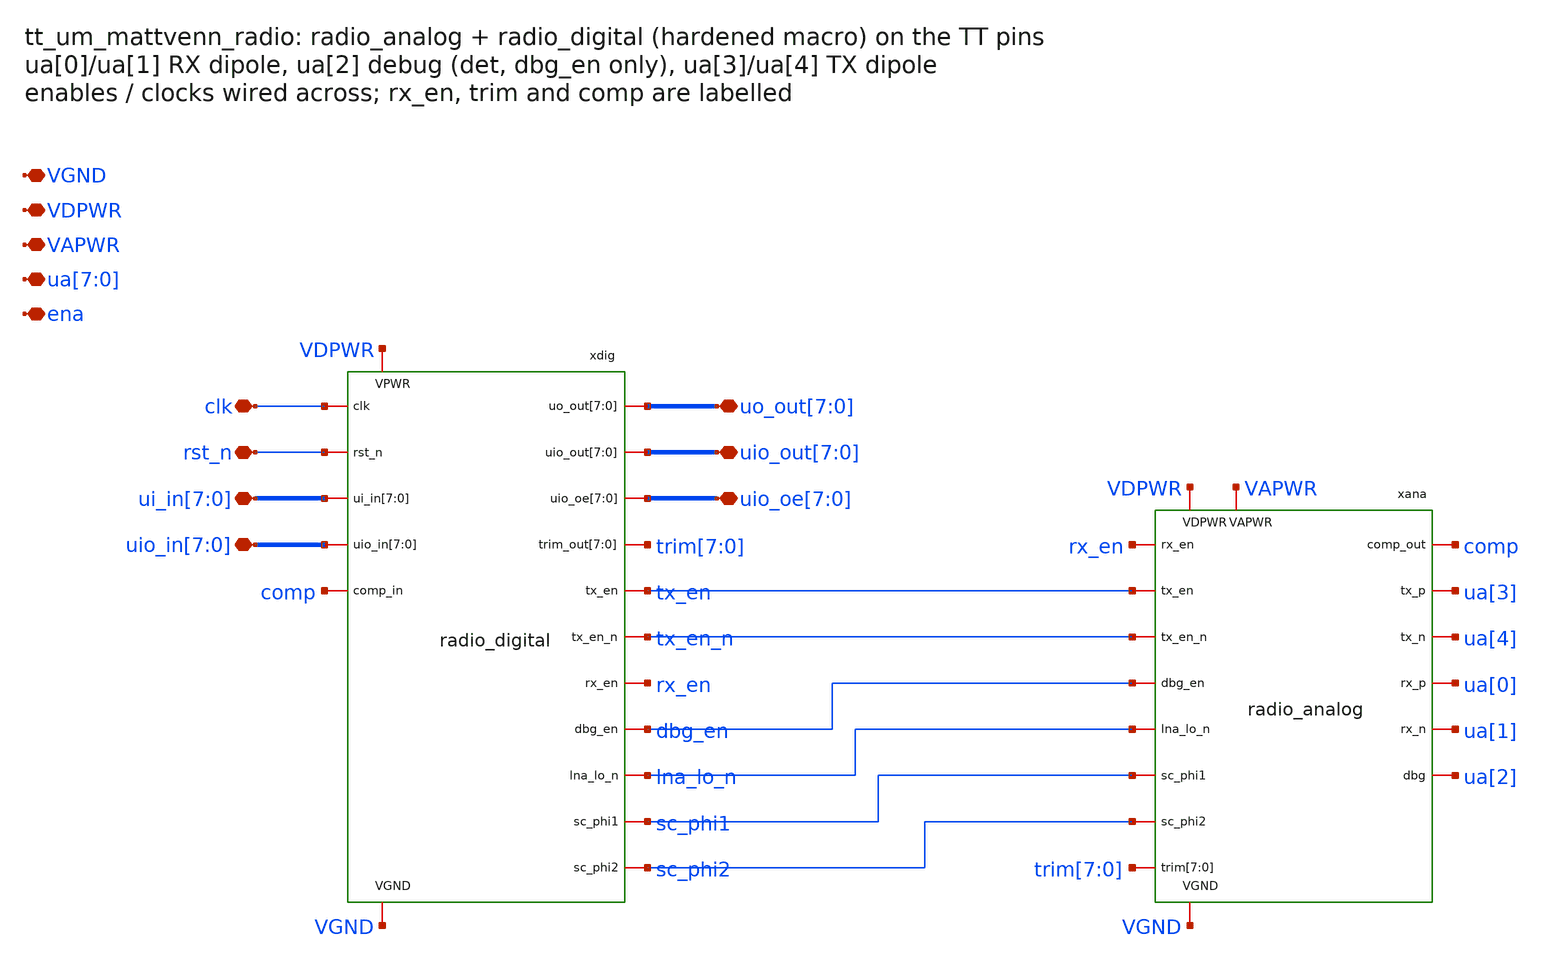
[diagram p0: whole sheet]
** sch_path: xschem/tt_um_mattvenn_radio.sch
**.subckt tt_um_mattvenn_radio VGND VDPWR VAPWR
*+ ui_in[7],ui_in[6],ui_in[5],ui_in[4],ui_in[3],ui_in[2],ui_in[1],ui_in[0] uo_out[7],uo_out[6],uo_out[5],uo_out[4],uo_out[3],uo_out[2],uo_out[1],uo_out[0]
*+ uio_in[7],uio_in[6],uio_in[5],uio_in[4],uio_in[3],uio_in[2],uio_in[1],uio_in[0] uio_out[7],uio_out[6],uio_out[5],uio_out[4],uio_out[3],uio_out[2],uio_out[1],uio_out[0]
*+ uio_oe[7],uio_oe[6],uio_oe[5],uio_oe[4],uio_oe[3],uio_oe[2],uio_oe[1],uio_oe[0] ua[7],ua[6],ua[5],ua[4],ua[3],ua[2],ua[1],ua[0] ena clk rst_n
*.iopin VGND
*.iopin VDPWR
*.iopin VAPWR
*.iopin ui_in[7],ui_in[6],ui_in[5],ui_in[4],ui_in[3],ui_in[2],ui_in[1],ui_in[0]
*.iopin uo_out[7],uo_out[6],uo_out[5],uo_out[4],uo_out[3],uo_out[2],uo_out[1],uo_out[0]
*.iopin uio_in[7],uio_in[6],uio_in[5],uio_in[4],uio_in[3],uio_in[2],uio_in[1],uio_in[0]
*.iopin uio_out[7],uio_out[6],uio_out[5],uio_out[4],uio_out[3],uio_out[2],uio_out[1],uio_out[0]
*.iopin uio_oe[7],uio_oe[6],uio_oe[5],uio_oe[4],uio_oe[3],uio_oe[2],uio_oe[1],uio_oe[0]
*.iopin ua[7],ua[6],ua[5],ua[4],ua[3],ua[2],ua[1],ua[0]
*.iopin ena
*.iopin clk
*.iopin rst_n
xdig clk rst_n ui_in[7] ui_in[6] ui_in[5] ui_in[4] ui_in[3] ui_in[2] ui_in[1] ui_in[0] uio_in[7]
+ uio_in[6] uio_in[5] uio_in[4] uio_in[3] uio_in[2] uio_in[1] uio_in[0] comp uo_out[7] uo_out[6] uo_out[5]
+ uo_out[4] uo_out[3] uo_out[2] uo_out[1] uo_out[0] uio_out[7] uio_out[6] uio_out[5] uio_out[4] uio_out[3]
+ uio_out[2] uio_out[1] uio_out[0] uio_oe[7] uio_oe[6] uio_oe[5] uio_oe[4] uio_oe[3] uio_oe[2] uio_oe[1]
+ uio_oe[0] trim[7] trim[6] trim[5] trim[4] trim[3] trim[2] trim[1] trim[0] tx_en tx_en_n rx_en dbg_en lna_lo_n
+ sc_phi1 sc_phi2 VDPWR VGND radio_digital
xana rx_en tx_en tx_en_n dbg_en lna_lo_n sc_phi1 sc_phi2 trim[7] trim[6] trim[5] trim[4] trim[3]
+ trim[2] trim[1] trim[0] comp ua[3] ua[4] ua[0] ua[1] ua[2] VDPWR VAPWR VGND radio_analog
**.ends

* expanding   symbol:  radio_digital.sym # of pins=18
** sym_path: xschem/radio_digital.sym
** radio_digital: hardened macro (openlane/radio_digital); gate-level netlist from the OpenLane run

* expanding   symbol:  radio_analog.sym # of pins=17
** sym_path: xschem/radio_analog.sym
** sch_path: xschem/radio_analog.sch
.subckt radio_analog rx_en tx_en tx_en_n dbg_en lna_lo_n sc_phi1 sc_phi2 trim[7] trim[6] trim[5]
+ trim[4] trim[3] trim[2] trim[1] trim[0] comp_out tx_p tx_n rx_p rx_n dbg VDPWR VAPWR VGND
*.iopin VDPWR
*.iopin VAPWR
*.iopin VGND
*.iopin rx_en
*.iopin tx_en
*.iopin tx_en_n
*.iopin dbg_en
*.iopin lna_lo_n
*.iopin sc_phi1
*.iopin sc_phi2
*.iopin trim[7],trim[6],trim[5],trim[4],trim[3],trim[2],trim[1],trim[0]
*.iopin comp_out
*.iopin tx_p
*.iopin tx_n
*.iopin rx_p
*.iopin rx_n
*.iopin dbg
xbias rx_en vcm ib_chain ib_det ib_comp VDPWR VGND bias_gen rref=10k rdiv=200k rtail=250k wpu=2
+ cc=1p
xchain rx_p rx_n ib_chain vcm lna_lo_n out_p out_n o1p o1n o2p o2n o3p o3n o4p o4n o5p o5n VDPWR
+ VGND lna_chain w1=80 rl1=1k mt1=20 w2=20 rl2=4k mt2=6 cs=0.6p cin=2p rb=20k mm=0
xdet o1p o1n o2p o2n o3p o3n o4p o4n o5p o5n out_p out_n ib_det det VDPWR VGND log_det wd=1 rs=10k
+ cc=100f rb=200k rdet=8k cdet=5p
xlpf det lpf VGND lpf_rc lr=136 nc=6
xavg lpf sc_phi1 sc_phi2 avg VDPWR VGND avg_sc ncs=1 nca=5
xdac trim[0] trim[1] trim[2] trim[3] trim[4] trim[5] trim[6] trim[7] trim VGND r2r
XCtrim trim VGND sky130_fd_pr__cap_mim_m3_1 W='sqrt((1e-12)/1/2.06e-15)' L='sqrt((1e-12)/1/2.06e-15)'
+ MF=1 m=1
xcomp avg lpf trim ib_comp comp_out VDPWR VGND comp_ct w1=20 l1=1 mt1=10 rdeg=0.85Meg mta=2 lref1=68
+ lref2=204 wcl=22
xdbg det dbg_en dbg VDPWR VGND dbg_tg wn=2 wp=4
xtx tx_en tx_en tx_en_n tx_p tx_n VDPWR VAPWR VGND tx_top
xdeca VAPWR VGND decap_vapwr
xdecd VDPWR VGND decap_vdpwr
.ends


* expanding   symbol:  bias_gen.sym # of pins=7
** sym_path: xschem/bias_gen.sym
** sch_path: xschem/bias_gen.sch
.subckt bias_gen en vcm ib_chain ib_det ib_comp VDD VSS  rref=10k rdiv=200k rtail=250k wpu=2 cc=1p
*.iopin VDD
*.iopin VSS
*.iopin en
*.iopin vcm
*.iopin ib_chain
*.iopin ib_det
*.iopin ib_comp
XMeip enb en VDD VDD sky130_fd_pr__pfet_01v8 L=0.15 W=1 nf=1 ad='int((nf+1)/2) * W/nf * 0.29' as='int((nf+2)/2) * W/nf * 0.29'
+ pd='2*int((nf+1)/2) * (W/nf + 0.29)' ps='2*int((nf+2)/2) * (W/nf + 0.29)' nrd='0.29 / W' nrs='0.29 / W'
+ sa=0 sb=0 sd=0 mult=1 m=1
XMein enb en VSS VSS sky130_fd_pr__nfet_01v8 L=0.15 W=0.5 nf=1 ad='int((nf+1)/2) * W/nf * 0.29' as='int((nf+2)/2) * W/nf * 0.29'
+ pd='2*int((nf+1)/2) * (W/nf + 0.29)' ps='2*int((nf+2)/2) * (W/nf + 0.29)' nrd='0.29 / W' nrs='0.29 / W'
+ sa=0 sb=0 sd=0 mult=1 m=1
XRd1 vcm VDD VSS sky130_fd_pr__res_xhigh_po_0p35 L='max((rdiv-0)/7379,0.5)' mult=1 m=1
XRd2 vref vcm VSS sky130_fd_pr__res_xhigh_po_0p35 L='max((rdiv-0)/7379,0.5)' mult=1 m=1
XRd3 dsw vref VSS sky130_fd_pr__res_xhigh_po_0p35 L='max((rdiv-0)/7379,0.5)' mult=1 m=1
XMdsw dsw en VSS VSS sky130_fd_pr__nfet_01v8 L=0.15 W=1 nf=1 ad='int((nf+1)/2) * W/nf * 0.29' as='int((nf+2)/2) * W/nf * 0.29'
+ pd='2*int((nf+1)/2) * (W/nf + 0.29)' ps='2*int((nf+2)/2) * (W/nf + 0.29)' nrd='0.29 / W' nrs='0.29 / W'
+ sa=0 sb=0 sd=0 mult=1 m=1
XCvcm vcm VSS sky130_fd_pr__cap_mim_m3_1 W='sqrt((2e-12)/2/2.06e-15)' L='sqrt((2e-12)/2/2.06e-15)' MF=2
+ m=2
XCvref vref VSS sky130_fd_pr__cap_mim_m3_1 W='sqrt((2e-12)/2/2.06e-15)' L='sqrt((2e-12)/2/2.06e-15)'
+ MF=2 m=2
XMpb pb pb VDD VDD sky130_fd_pr__pfet_01v8 L=1 W=4 nf=1 ad='int((nf+1)/2) * W/nf * 0.29' as='int((nf+2)/2) * W/nf * 0.29'
+ pd='2*int((nf+1)/2) * (W/nf + 0.29)' ps='2*int((nf+2)/2) * (W/nf + 0.29)' nrd='0.29 / W' nrs='0.29 / W'
+ sa=0 sb=0 sd=0 mult=1 m=1
XRtail tsw pb VSS sky130_fd_pr__res_xhigh_po_0p35 L='max((rtail-0)/7379,0.5)' mult=1 m=1
XMtsw tsw en VSS VSS sky130_fd_pr__nfet_01v8 L=0.15 W=1 nf=1 ad='int((nf+1)/2) * W/nf * 0.29' as='int((nf+2)/2) * W/nf * 0.29'
+ pd='2*int((nf+1)/2) * (W/nf + 0.29)' ps='2*int((nf+2)/2) * (W/nf + 0.29)' nrd='0.29 / W' nrs='0.29 / W'
+ sa=0 sb=0 sd=0 mult=1 m=1
XMpt tail pb VDD VDD sky130_fd_pr__pfet_01v8 L=1 W=4 nf=1 ad='int((nf+1)/2) * W/nf * 0.29' as='int((nf+2)/2) * W/nf * 0.29'
+ pd='2*int((nf+1)/2) * (W/nf + 0.29)' ps='2*int((nf+2)/2) * (W/nf + 0.29)' nrd='0.29 / W' nrs='0.29 / W'
+ sa=0 sb=0 sd=0 mult=1 m=1
XM1 d1 vref tail VDD sky130_fd_pr__pfet_01v8 L=1 W=4 nf=1 ad='int((nf+1)/2) * W/nf * 0.29' as='int((nf+2)/2) * W/nf * 0.29'
+ pd='2*int((nf+1)/2) * (W/nf + 0.29)' ps='2*int((nf+2)/2) * (W/nf + 0.29)' nrd='0.29 / W' nrs='0.29 / W'
+ sa=0 sb=0 sd=0 mult=1 m=1
XM2 ota x tail VDD sky130_fd_pr__pfet_01v8 L=1 W=4 nf=1 ad='int((nf+1)/2) * W/nf * 0.29' as='int((nf+2)/2) * W/nf * 0.29'
+ pd='2*int((nf+1)/2) * (W/nf + 0.29)' ps='2*int((nf+2)/2) * (W/nf + 0.29)' nrd='0.29 / W' nrs='0.29 / W'
+ sa=0 sb=0 sd=0 mult=1 m=1
XM3 d1 d1 VSS VSS sky130_fd_pr__nfet_01v8 L=2 W=2 nf=1 ad='int((nf+1)/2) * W/nf * 0.29' as='int((nf+2)/2) * W/nf * 0.29'
+ pd='2*int((nf+1)/2) * (W/nf + 0.29)' ps='2*int((nf+2)/2) * (W/nf + 0.29)' nrd='0.29 / W' nrs='0.29 / W'
+ sa=0 sb=0 sd=0 mult=1 m=1
XM4 ota d1 VSS VSS sky130_fd_pr__nfet_01v8 L=2 W=2 nf=1 ad='int((nf+1)/2) * W/nf * 0.29' as='int((nf+2)/2) * W/nf * 0.29'
+ pd='2*int((nf+1)/2) * (W/nf + 0.29)' ps='2*int((nf+2)/2) * (W/nf + 0.29)' nrd='0.29 / W' nrs='0.29 / W'
+ sa=0 sb=0 sd=0 mult=1 m=1
XCc ota VSS sky130_fd_pr__cap_mim_m3_1 W='sqrt((cc)/1/2.06e-15)' L='sqrt((cc)/1/2.06e-15)' MF=1 m=1
XMpd ota enb VSS VSS sky130_fd_pr__nfet_01v8 L=0.15 W=1 nf=1 ad='int((nf+1)/2) * W/nf * 0.29' as='int((nf+2)/2) * W/nf * 0.29'
+ pd='2*int((nf+1)/2) * (W/nf + 0.29)' ps='2*int((nf+2)/2) * (W/nf + 0.29)' nrd='0.29 / W' nrs='0.29 / W'
+ sa=0 sb=0 sd=0 mult=1 m=1
XMn pr ota x VSS sky130_fd_pr__nfet_01v8 L=0.5 W=20 nf=2 ad='int((nf+1)/2) * W/nf * 0.29' as='int((nf+2)/2) * W/nf * 0.29'
+ pd='2*int((nf+1)/2) * (W/nf + 0.29)' ps='2*int((nf+2)/2) * (W/nf + 0.29)' nrd='0.29 / W' nrs='0.29 / W'
+ sa=0 sb=0 sd=0 mult=1 m=1
XRref1 xr x VSS sky130_fd_pr__res_high_po_0p69 L='max((rref/2-526)/470.9,0.5)' mult=1 m=1
XRref2 VSS xr VSS sky130_fd_pr__res_high_po_0p69 L='max((rref/2-526)/470.9,0.5)' mult=1 m=1
XMpr pr pr VDD VDD sky130_fd_pr__pfet_01v8 L=1 W='wpu' nf=1 ad='int((nf+1)/2) * W/nf * 0.29' as='int((nf+2)/2) * W/nf * 0.29'
+ pd='2*int((nf+1)/2) * (W/nf + 0.29)' ps='2*int((nf+2)/2) * (W/nf + 0.29)' nrd='0.29 / W' nrs='0.29 / W'
+ sa=0 sb=0 sd=0 mult=60 m=60
XMpu pr en VDD VDD sky130_fd_pr__pfet_01v8 L=0.15 W=1 nf=1 ad='int((nf+1)/2) * W/nf * 0.29' as='int((nf+2)/2) * W/nf * 0.29'
+ pd='2*int((nf+1)/2) * (W/nf + 0.29)' ps='2*int((nf+2)/2) * (W/nf + 0.29)' nrd='0.29 / W' nrs='0.29 / W'
+ sa=0 sb=0 sd=0 mult=1 m=1
XMo_ib_chain ib_chain pr VDD VDD sky130_fd_pr__pfet_01v8 L=1 W='wpu' nf=1 ad='int((nf+1)/2) * W/nf * 0.29'
+ as='int((nf+2)/2) * W/nf * 0.29' pd='2*int((nf+1)/2) * (W/nf + 0.29)' ps='2*int((nf+2)/2) * (W/nf + 0.29)'
+ nrd='0.29 / W' nrs='0.29 / W' sa=0 sb=0 sd=0 mult=60 m=60
XMo_ib_det ib_det pr VDD VDD sky130_fd_pr__pfet_01v8 L=1 W='wpu' nf=1 ad='int((nf+1)/2) * W/nf * 0.29'
+ as='int((nf+2)/2) * W/nf * 0.29' pd='2*int((nf+1)/2) * (W/nf + 0.29)' ps='2*int((nf+2)/2) * (W/nf + 0.29)'
+ nrd='0.29 / W' nrs='0.29 / W' sa=0 sb=0 sd=0 mult=2 m=2
XMo_ib_comp ib_comp pr VDD VDD sky130_fd_pr__pfet_01v8 L=1 W='wpu' nf=1 ad='int((nf+1)/2) * W/nf * 0.29'
+ as='int((nf+2)/2) * W/nf * 0.29' pd='2*int((nf+1)/2) * (W/nf + 0.29)' ps='2*int((nf+2)/2) * (W/nf + 0.29)'
+ nrd='0.29 / W' nrs='0.29 / W' sa=0 sb=0 sd=0 mult=1 m=1
XMdum VDD VDD VDD VDD sky130_fd_pr__pfet_01v8 L=1 W='wpu' nf=1 ad='int((nf+1)/2) * W/nf * 0.29' as='int((nf+2)/2) * W/nf * 0.29'
+ pd='2*int((nf+1)/2) * (W/nf + 0.29)' ps='2*int((nf+2)/2) * (W/nf + 0.29)' nrd='0.29 / W' nrs='0.29 / W'
+ sa=0 sb=0 sd=0 mult=5 m=5
.ends


* expanding   symbol:  lna_chain.sym # of pins=19
** sym_path: xschem/lna_chain.sym
** sch_path: xschem/lna_chain.sch
.subckt lna_chain inp inn ibias vcm lna_lo_n outp outn o1p o1n o2p o2n o3p o3n o4p o4n o5p o5n VDD
+ VSS  w1=80 rl1=1k mt1=20 w2=20 rl2=4k mt2=6 cs=0.6p cin=2p rb=20k mm=0
*.iopin VDD
*.iopin VSS
*.iopin ibias
*.iopin vcm
*.iopin lna_lo_n
*.iopin inp
*.iopin inn
*.iopin outp
*.iopin outn
*.iopin o1p
*.iopin o1n
*.iopin o2p
*.iopin o2n
*.iopin o3p
*.iopin o3n
*.iopin o4p
*.iopin o4n
*.iopin o5p
*.iopin o5n
XMref ibias ibias VSS VSS sky130_fd_pr__nfet_01v8 L=0.5 W=6 nf=2 ad='int((nf+1)/2) * W/nf * 0.29' as='int((nf+2)/2) * W/nf * 0.29'
+ pd='2*int((nf+1)/2) * (W/nf + 0.29)' ps='2*int((nf+2)/2) * (W/nf + 0.29)' nrd='0.29 / W' nrs='0.29 / W'
+ sa=0 sb=0 sd=0 mult=1 m=1
XCin_p g1p inp sky130_fd_pr__cap_mim_m3_1 W='sqrt((cin)/2.06e-15/3.84131)' L='3.84131*sqrt((cin)/2.06e-15/3.84131)'
+ MF=1 m=1
XRb_p g1p vcm VSS sky130_fd_pr__res_high_po_0p35 L='max((rb-963)/995,0.5)' mult=1 m=1
XCin_n g1n inn sky130_fd_pr__cap_mim_m3_1 W='sqrt((cin)/2.06e-15/3.84131)' L='3.84131*sqrt((cin)/2.06e-15/3.84131)'
+ MF=1 m=1
XRb_n g1n vcm VSS sky130_fd_pr__res_high_po_0p35 L='max((rb-963)/995,0.5)' mult=1 m=1
xa1 g1p g1n ibias o1p o1n VDD VSS amp_dp w='w1' l=0.15 rl='rl1' wt=6 mt='mt1' mm='mm'
xa2 o1p o1n ibias o2p o2n VDD VSS amp_dpc w='w2' l=0.15 rl='rl2' wt=6 mt='mt2' cs='cs'
xa3 o2p o2n ibias o3p o3n VDD VSS amp_dpc w='w2' l=0.15 rl='rl2' wt=6 mt='mt2' cs='cs'
xa4 o3p o3n ibias o4p o4n VDD VSS amp_dpc w='w2' l=0.15 rl='rl2' wt=6 mt='mt2' cs='cs'
xa5 o4p o4n ibias o5p o5n VDD VSS amp_dpc w='w2' l=0.15 rl='rl2' wt=6 mt='mt2' cs='cs'
xa6 o5p o5n ibias outp outn VDD VSS amp_dpc w='w2' l=0.15 rl='rl2' wt=6 mt='mt2' cs='cs'
xsh o2p o2n lna_lo_n VDD VSS lna_shunt rh=421 wsw=18 rg=20k
.ends


* expanding   symbol:  log_det.sym # of pins=16
** sym_path: xschem/log_det.sym
** sch_path: xschem/log_det.sch
.subckt log_det t1p t1n t2p t2n t3p t3n t4p t4n t5p t5n t6p t6n ibias_det det VDD VSS  wd=1 rs=10k
+ cc=100f rb=200k rdet=8k cdet=5p
*.iopin VDD
*.iopin VSS
*.iopin ibias_det
*.iopin det
*.iopin t1p
*.iopin t1n
*.iopin t2p
*.iopin t2n
*.iopin t3p
*.iopin t3n
*.iopin t4p
*.iopin t4n
*.iopin t5p
*.iopin t5n
*.iopin t6p
*.iopin t6n
XMbias ibias_det ibias_det sb VSS sky130_fd_pr__nfet_01v8 L=0.15 W='wd' nf=1 ad='int((nf+1)/2) * W/nf * 0.29'
+ as='int((nf+2)/2) * W/nf * 0.29' pd='2*int((nf+1)/2) * (W/nf + 0.29)' ps='2*int((nf+2)/2) * (W/nf + 0.29)'
+ nrd='0.29 / W' nrs='0.29 / W' sa=0 sb=0 sd=0 mult=1 m=1
XRs_b VSS sb VSS sky130_fd_pr__res_high_po_0p35 L='max((rs-963)/995,0.5)' mult=1 m=1
XRdet det VDD VSS sky130_fd_pr__res_high_po_0p69 L='max((rdet-526)/470.9,0.5)' mult=1 m=1
XCdet det VDD sky130_fd_pr__cap_mim_m3_1 W='sqrt((cdet)/1/2.06e-15)' L='sqrt((cdet)/1/2.06e-15)' MF=1
+ m=1
xd1 t1p t1n ibias_det det VSS det_cell wd='wd' rs='rs' cc='cc' rb='rb'
xd2 t2p t2n ibias_det det VSS det_cell wd='wd' rs='rs' cc='cc' rb='rb'
xd3 t3p t3n ibias_det det VSS det_cell wd='wd' rs='rs' cc='cc' rb='rb'
xd4 t4p t4n ibias_det det VSS det_cell wd='wd' rs='rs' cc='cc' rb='rb'
xd5 t5p t5n ibias_det det VSS det_cell wd='wd' rs='rs' cc='cc' rb='rb'
xd6 t6p t6n ibias_det det VSS det_cell wd='wd' rs='rs' cc='cc' rb='rb'
.ends


* expanding   symbol:  lpf_rc.sym # of pins=3
** sym_path: xschem/lpf_rc.sym
** sch_path: xschem/lpf_rc.sch
.subckt lpf_rc in out VSS  lr=136 nc=6
*.iopin VSS
*.iopin in
*.iopin out
XR1 in out VSS sky130_fd_pr__res_xhigh_po_0p35 L='lr' mult=1 m=1
XC1 out VSS sky130_fd_pr__cap_mim_m3_1 W=30 L=30 MF='nc' m='nc'
.ends


* expanding   symbol:  avg_sc.sym # of pins=6
** sym_path: xschem/avg_sc.sym
** sch_path: xschem/avg_sc.sch
.subckt avg_sc in phi1 phi2 out VDD VSS  ncs=1 nca=5
*.iopin VDD
*.iopin VSS
*.iopin in
*.iopin out
*.iopin phi1
*.iopin phi2
XMiphi1p phi1b phi1 VDD VDD sky130_fd_pr__pfet_01v8 L=0.15 W=1 nf=1 ad='int((nf+1)/2) * W/nf * 0.29'
+ as='int((nf+2)/2) * W/nf * 0.29' pd='2*int((nf+1)/2) * (W/nf + 0.29)' ps='2*int((nf+2)/2) * (W/nf + 0.29)'
+ nrd='0.29 / W' nrs='0.29 / W' sa=0 sb=0 sd=0 mult=1 m=1
XMiphi1n phi1b phi1 VSS VSS sky130_fd_pr__nfet_01v8 L=0.15 W=0.5 nf=1 ad='int((nf+1)/2) * W/nf * 0.29'
+ as='int((nf+2)/2) * W/nf * 0.29' pd='2*int((nf+1)/2) * (W/nf + 0.29)' ps='2*int((nf+2)/2) * (W/nf + 0.29)'
+ nrd='0.29 / W' nrs='0.29 / W' sa=0 sb=0 sd=0 mult=1 m=1
XMiphi2p phi2b phi2 VDD VDD sky130_fd_pr__pfet_01v8 L=0.15 W=1 nf=1 ad='int((nf+1)/2) * W/nf * 0.29'
+ as='int((nf+2)/2) * W/nf * 0.29' pd='2*int((nf+1)/2) * (W/nf + 0.29)' ps='2*int((nf+2)/2) * (W/nf + 0.29)'
+ nrd='0.29 / W' nrs='0.29 / W' sa=0 sb=0 sd=0 mult=1 m=1
XMiphi2n phi2b phi2 VSS VSS sky130_fd_pr__nfet_01v8 L=0.15 W=0.5 nf=1 ad='int((nf+1)/2) * W/nf * 0.29'
+ as='int((nf+2)/2) * W/nf * 0.29' pd='2*int((nf+1)/2) * (W/nf + 0.29)' ps='2*int((nf+2)/2) * (W/nf + 0.29)'
+ nrd='0.29 / W' nrs='0.29 / W' sa=0 sb=0 sd=0 mult=1 m=1
XS1n in phi1 cs VSS sky130_fd_pr__nfet_01v8 L=0.15 W=0.5 nf=1 ad='int((nf+1)/2) * W/nf * 0.29' as='int((nf+2)/2) * W/nf * 0.29'
+ pd='2*int((nf+1)/2) * (W/nf + 0.29)' ps='2*int((nf+2)/2) * (W/nf + 0.29)' nrd='0.29 / W' nrs='0.29 / W'
+ sa=0 sb=0 sd=0 mult=1 m=1
XS1p in phi1b cs VDD sky130_fd_pr__pfet_01v8 L=0.15 W=1 nf=1 ad='int((nf+1)/2) * W/nf * 0.29' as='int((nf+2)/2) * W/nf * 0.29'
+ pd='2*int((nf+1)/2) * (W/nf + 0.29)' ps='2*int((nf+2)/2) * (W/nf + 0.29)' nrd='0.29 / W' nrs='0.29 / W'
+ sa=0 sb=0 sd=0 mult=1 m=1
XS2n cs phi2 out VSS sky130_fd_pr__nfet_01v8 L=0.15 W=0.5 nf=1 ad='int((nf+1)/2) * W/nf * 0.29' as='int((nf+2)/2) * W/nf * 0.29'
+ pd='2*int((nf+1)/2) * (W/nf + 0.29)' ps='2*int((nf+2)/2) * (W/nf + 0.29)' nrd='0.29 / W' nrs='0.29 / W'
+ sa=0 sb=0 sd=0 mult=1 m=1
XS2p cs phi2b out VDD sky130_fd_pr__pfet_01v8 L=0.15 W=1 nf=1 ad='int((nf+1)/2) * W/nf * 0.29' as='int((nf+2)/2) * W/nf * 0.29'
+ pd='2*int((nf+1)/2) * (W/nf + 0.29)' ps='2*int((nf+2)/2) * (W/nf + 0.29)' nrd='0.29 / W' nrs='0.29 / W'
+ sa=0 sb=0 sd=0 mult=1 m=1
XCs cs VSS sky130_fd_pr__cap_mim_m3_1 W='wcs' L='wcs' MF='ncs' m='ncs'
XCavg out VSS sky130_fd_pr__cap_mim_m3_1 W=30 L=30 MF='nca' m='nca'
.ends


* expanding   symbol:  r2r.sym # of pins=10
** sym_path: xschem/r2r.sym
** sch_path: xschem/r2r.sch
.subckt r2r b0 b1 b2 b3 b4 b5 b6 b7 out VGND
*.iopin b0
*.iopin b1
*.iopin b2
*.iopin b3
*.iopin b4
*.iopin b5
*.iopin b6
*.iopin b7
*.iopin out
*.iopin VGND
XR1 s0 b0 VGND sky130_fd_pr__res_high_po_1p41 L=45 mult=1 m=1
XR2 a0 s0 VGND sky130_fd_pr__res_high_po_1p41 L=45 mult=1 m=1
XR3 s1 a0 VGND sky130_fd_pr__res_high_po_1p41 L=45 mult=1 m=1
XR4 VGND s1 VGND sky130_fd_pr__res_high_po_1p41 L=45 mult=1 m=1
XR5 VGND VGND VGND sky130_fd_pr__res_high_po_1p41 L=45 mult=1 m=1
XR6 a1 a0 VGND sky130_fd_pr__res_high_po_1p41 L=45 mult=1 m=1
XR7 t1 a1 VGND sky130_fd_pr__res_high_po_1p41 L=45 mult=1 m=1
XR8 b1 t1 VGND sky130_fd_pr__res_high_po_1p41 L=45 mult=1 m=1
XR9 a2 a1 VGND sky130_fd_pr__res_high_po_1p41 L=45 mult=1 m=1
XR10 t2 a2 VGND sky130_fd_pr__res_high_po_1p41 L=45 mult=1 m=1
XR11 b2 t2 VGND sky130_fd_pr__res_high_po_1p41 L=45 mult=1 m=1
XR12 a3 a2 VGND sky130_fd_pr__res_high_po_1p41 L=45 mult=1 m=1
XR13 t3 a3 VGND sky130_fd_pr__res_high_po_1p41 L=45 mult=1 m=1
XR14 b3 t3 VGND sky130_fd_pr__res_high_po_1p41 L=45 mult=1 m=1
XR15 a4 a3 VGND sky130_fd_pr__res_high_po_1p41 L=45 mult=1 m=1
XR16 t4 a4 VGND sky130_fd_pr__res_high_po_1p41 L=45 mult=1 m=1
XR17 b4 t4 VGND sky130_fd_pr__res_high_po_1p41 L=45 mult=1 m=1
XR18 a5 a4 VGND sky130_fd_pr__res_high_po_1p41 L=45 mult=1 m=1
XR19 t5 a5 VGND sky130_fd_pr__res_high_po_1p41 L=45 mult=1 m=1
XR20 b5 t5 VGND sky130_fd_pr__res_high_po_1p41 L=45 mult=1 m=1
XR21 a6 a5 VGND sky130_fd_pr__res_high_po_1p41 L=45 mult=1 m=1
XR22 t6 a6 VGND sky130_fd_pr__res_high_po_1p41 L=45 mult=1 m=1
XR23 b6 t6 VGND sky130_fd_pr__res_high_po_1p41 L=45 mult=1 m=1
XR24 out a6 VGND sky130_fd_pr__res_high_po_1p41 L=45 mult=1 m=1
XR25 t7 out VGND sky130_fd_pr__res_high_po_1p41 L=45 mult=1 m=1
XR26 b7 t7 VGND sky130_fd_pr__res_high_po_1p41 L=45 mult=1 m=1
XR27 VGND VGND VGND sky130_fd_pr__res_high_po_1p41 L=45 mult=1 m=1
.ends


* expanding   symbol:  comp_ct.sym # of pins=7
** sym_path: xschem/comp_ct.sym
** sch_path: xschem/comp_ct.sch
.subckt comp_ct inp inn trim ibias out VDD VSS  w1=20 l1=1 mt1=10 rdeg=0.85Meg mta=2 lref1=68
+ lref2=204 wcl=22
*.iopin VDD
*.iopin VSS
*.iopin ibias
*.iopin inp
*.iopin inn
*.iopin trim
*.iopin out
XMb ibias ibias VSS VSS sky130_fd_pr__nfet_01v8 L=2 W=2 nf=1 ad='int((nf+1)/2) * W/nf * 0.29' as='int((nf+2)/2) * W/nf * 0.29'
+ pd='2*int((nf+1)/2) * (W/nf + 0.29)' ps='2*int((nf+2)/2) * (W/nf + 0.29)' nrd='0.29 / W' nrs='0.29 / W'
+ sa=0 sb=0 sd=0 mult=1 m=1
XMt1 tail ibias VSS VSS sky130_fd_pr__nfet_01v8 L=2 W='0.455*mt1' nf=1 ad='int((nf+1)/2) * W/nf * 0.29'
+ as='int((nf+2)/2) * W/nf * 0.29' pd='2*int((nf+1)/2) * (W/nf + 0.29)' ps='2*int((nf+2)/2) * (W/nf + 0.29)'
+ nrd='0.29 / W' nrs='0.29 / W' sa=0 sb=0 sd=0 mult=4 m=4
XM1 d1 inp tail VSS sky130_fd_pr__nfet_01v8_lvt L='l1' W='w1' nf=4 ad='int((nf+1)/2) * W/nf * 0.29' as='int((nf+2)/2) * W/nf * 0.29'
+ pd='2*int((nf+1)/2) * (W/nf + 0.29)' ps='2*int((nf+2)/2) * (W/nf + 0.29)' nrd='0.29 / W' nrs='0.29 / W'
+ sa=0 sb=0 sd=0 mult=1 m=1
XM2 d2 inn tail VSS sky130_fd_pr__nfet_01v8_lvt L='l1' W='w1' nf=4 ad='int((nf+1)/2) * W/nf * 0.29' as='int((nf+2)/2) * W/nf * 0.29'
+ pd='2*int((nf+1)/2) * (W/nf + 0.29)' ps='2*int((nf+2)/2) * (W/nf + 0.29)' nrd='0.29 / W' nrs='0.29 / W'
+ sa=0 sb=0 sd=0 mult=1 m=1
XMp1 d1 d1 VDD VDD sky130_fd_pr__pfet_01v8_lvt L=2 W=8 nf=1 ad='int((nf+1)/2) * W/nf * 0.29' as='int((nf+2)/2) * W/nf * 0.29'
+ pd='2*int((nf+1)/2) * (W/nf + 0.29)' ps='2*int((nf+2)/2) * (W/nf + 0.29)' nrd='0.29 / W' nrs='0.29 / W'
+ sa=0 sb=0 sd=0 mult=1 m=1
XMp2 d2 d1 VDD VDD sky130_fd_pr__pfet_01v8_lvt L=2 W=8 nf=1 ad='int((nf+1)/2) * W/nf * 0.29' as='int((nf+2)/2) * W/nf * 0.29'
+ pd='2*int((nf+1)/2) * (W/nf + 0.29)' ps='2*int((nf+2)/2) * (W/nf + 0.29)' nrd='0.29 / W' nrs='0.29 / W'
+ sa=0 sb=0 sd=0 mult=1 m=1
XM3 d1 vref sa VSS sky130_fd_pr__nfet_01v8_lvt L=1 W=8 nf=1 ad='int((nf+1)/2) * W/nf * 0.29' as='int((nf+2)/2) * W/nf * 0.29'
+ pd='2*int((nf+1)/2) * (W/nf + 0.29)' ps='2*int((nf+2)/2) * (W/nf + 0.29)' nrd='0.29 / W' nrs='0.29 / W'
+ sa=0 sb=0 sd=0 mult=1 m=1
XMta_sa sa ibias VSS VSS sky130_fd_pr__nfet_01v8 L=2 W=2 nf=1 ad='int((nf+1)/2) * W/nf * 0.29' as='int((nf+2)/2) * W/nf * 0.29'
+ pd='2*int((nf+1)/2) * (W/nf + 0.29)' ps='2*int((nf+2)/2) * (W/nf + 0.29)' nrd='0.29 / W' nrs='0.29 / W'
+ sa=0 sb=0 sd=0 mult='mta' m='mta'
XM4 d2 trim sb VSS sky130_fd_pr__nfet_01v8_lvt L=1 W=8 nf=1 ad='int((nf+1)/2) * W/nf * 0.29' as='int((nf+2)/2) * W/nf * 0.29'
+ pd='2*int((nf+1)/2) * (W/nf + 0.29)' ps='2*int((nf+2)/2) * (W/nf + 0.29)' nrd='0.29 / W' nrs='0.29 / W'
+ sa=0 sb=0 sd=0 mult=1 m=1
XMta_sb sb ibias VSS VSS sky130_fd_pr__nfet_01v8 L=2 W=2 nf=1 ad='int((nf+1)/2) * W/nf * 0.29' as='int((nf+2)/2) * W/nf * 0.29'
+ pd='2*int((nf+1)/2) * (W/nf + 0.29)' ps='2*int((nf+2)/2) * (W/nf + 0.29)' nrd='0.29 / W' nrs='0.29 / W'
+ sa=0 sb=0 sd=0 mult='mta' m='mta'
XRdeg sa sb VSS sky130_fd_pr__res_xhigh_po_0p35 L='rdeg/7.37k' mult=1 m=1
XRr1 vref VDD VSS sky130_fd_pr__res_xhigh_po_0p35 L='lref1' mult=1 m=1
XRr2 VSS vref VSS sky130_fd_pr__res_xhigh_po_0p35 L='lref2' mult=1 m=1
XCref vref VSS sky130_fd_pr__cap_mim_m3_1 W=10 L=10 MF=1 m=1
XCl d2 VSS sky130_fd_pr__cap_mim_m3_1 W='wcl' L='wcl/2' MF=2 m=2
XMp3 o2 d2 VDD VDD sky130_fd_pr__pfet_01v8_lvt L=1 W=4 nf=1 ad='int((nf+1)/2) * W/nf * 0.29' as='int((nf+2)/2) * W/nf * 0.29'
+ pd='2*int((nf+1)/2) * (W/nf + 0.29)' ps='2*int((nf+2)/2) * (W/nf + 0.29)' nrd='0.29 / W' nrs='0.29 / W'
+ sa=0 sb=0 sd=0 mult=1 m=1
XMn3 o2 ibias VSS VSS sky130_fd_pr__nfet_01v8 L=2 W=4.55 nf=1 ad='int((nf+1)/2) * W/nf * 0.29' as='int((nf+2)/2) * W/nf * 0.29'
+ pd='2*int((nf+1)/2) * (W/nf + 0.29)' ps='2*int((nf+2)/2) * (W/nf + 0.29)' nrd='0.29 / W' nrs='0.29 / W'
+ sa=0 sb=0 sd=0 mult=2 m=2
XMip out o2 VDD VDD sky130_fd_pr__pfet_01v8 L=0.15 W=2 nf=1 ad='int((nf+1)/2) * W/nf * 0.29' as='int((nf+2)/2) * W/nf * 0.29'
+ pd='2*int((nf+1)/2) * (W/nf + 0.29)' ps='2*int((nf+2)/2) * (W/nf + 0.29)' nrd='0.29 / W' nrs='0.29 / W'
+ sa=0 sb=0 sd=0 mult=1 m=1
XMin out o2 VSS VSS sky130_fd_pr__nfet_01v8 L=0.15 W=1 nf=1 ad='int((nf+1)/2) * W/nf * 0.29' as='int((nf+2)/2) * W/nf * 0.29'
+ pd='2*int((nf+1)/2) * (W/nf + 0.29)' ps='2*int((nf+2)/2) * (W/nf + 0.29)' nrd='0.29 / W' nrs='0.29 / W'
+ sa=0 sb=0 sd=0 mult=1 m=1
XMdn1 VSS VSS VSS VSS sky130_fd_pr__nfet_01v8_lvt L=1 W=5 nf=1 ad='int((nf+1)/2) * W/nf * 0.29' as='int((nf+2)/2) * W/nf * 0.29'
+ pd='2*int((nf+1)/2) * (W/nf + 0.29)' ps='2*int((nf+2)/2) * (W/nf + 0.29)' nrd='0.29 / W' nrs='0.29 / W'
+ sa=0 sb=0 sd=0 mult=2 m=2
XMdn2 VSS VSS VSS VSS sky130_fd_pr__nfet_01v8_lvt L=1 W=4 nf=1 ad='int((nf+1)/2) * W/nf * 0.29' as='int((nf+2)/2) * W/nf * 0.29'
+ pd='2*int((nf+1)/2) * (W/nf + 0.29)' ps='2*int((nf+2)/2) * (W/nf + 0.29)' nrd='0.29 / W' nrs='0.29 / W'
+ sa=0 sb=0 sd=0 mult=2 m=2
XMdn3 VSS VSS VSS VSS sky130_fd_pr__nfet_01v8 L=2 W=2 nf=1 ad='int((nf+1)/2) * W/nf * 0.29' as='int((nf+2)/2) * W/nf * 0.29'
+ pd='2*int((nf+1)/2) * (W/nf + 0.29)' ps='2*int((nf+2)/2) * (W/nf + 0.29)' nrd='0.29 / W' nrs='0.29 / W'
+ sa=0 sb=0 sd=0 mult=1 m=1
XMdp1 VDD VDD VDD VDD sky130_fd_pr__pfet_01v8_lvt L=1 W=4 nf=1 ad='int((nf+1)/2) * W/nf * 0.29' as='int((nf+2)/2) * W/nf * 0.29'
+ pd='2*int((nf+1)/2) * (W/nf + 0.29)' ps='2*int((nf+2)/2) * (W/nf + 0.29)' nrd='0.29 / W' nrs='0.29 / W'
+ sa=0 sb=0 sd=0 mult=2 m=2
XMdp2 VDD VDD VDD VDD sky130_fd_pr__pfet_01v8_lvt L=1 W=4 nf=1 ad='int((nf+1)/2) * W/nf * 0.29' as='int((nf+2)/2) * W/nf * 0.29'
+ pd='2*int((nf+1)/2) * (W/nf + 0.29)' ps='2*int((nf+2)/2) * (W/nf + 0.29)' nrd='0.29 / W' nrs='0.29 / W'
+ sa=0 sb=0 sd=0 mult=1 m=1
.ends


* expanding   symbol:  dbg_tg.sym # of pins=5
** sym_path: xschem/dbg_tg.sym
** sch_path: xschem/dbg_tg.sch
.subckt dbg_tg a en b VDD VSS  wn=2 wp=4
*.iopin VDD
*.iopin VSS
*.iopin en
*.iopin a
*.iopin b
XMip enb en VDD VDD sky130_fd_pr__pfet_01v8 L=0.15 W=1 nf=1 ad='int((nf+1)/2) * W/nf * 0.29' as='int((nf+2)/2) * W/nf * 0.29'
+ pd='2*int((nf+1)/2) * (W/nf + 0.29)' ps='2*int((nf+2)/2) * (W/nf + 0.29)' nrd='0.29 / W' nrs='0.29 / W'
+ sa=0 sb=0 sd=0 mult=1 m=1
XMin enb en VSS VSS sky130_fd_pr__nfet_01v8 L=0.15 W=0.5 nf=1 ad='int((nf+1)/2) * W/nf * 0.29' as='int((nf+2)/2) * W/nf * 0.29'
+ pd='2*int((nf+1)/2) * (W/nf + 0.29)' ps='2*int((nf+2)/2) * (W/nf + 0.29)' nrd='0.29 / W' nrs='0.29 / W'
+ sa=0 sb=0 sd=0 mult=1 m=1
XMn a en b VSS sky130_fd_pr__nfet_01v8 L=0.15 W='wn' nf=1 ad='int((nf+1)/2) * W/nf * 0.29' as='int((nf+2)/2) * W/nf * 0.29'
+ pd='2*int((nf+1)/2) * (W/nf + 0.29)' ps='2*int((nf+2)/2) * (W/nf + 0.29)' nrd='0.29 / W' nrs='0.29 / W'
+ sa=0 sb=0 sd=0 mult=1 m=1
XMp a enb b VDD sky130_fd_pr__pfet_01v8 L=0.15 W='wp' nf=1 ad='int((nf+1)/2) * W/nf * 0.29' as='int((nf+2)/2) * W/nf * 0.29'
+ pd='2*int((nf+1)/2) * (W/nf + 0.29)' ps='2*int((nf+2)/2) * (W/nf + 0.29)' nrd='0.29 / W' nrs='0.29 / W'
+ sa=0 sb=0 sd=0 mult=1 m=1
.ends


* expanding   symbol:  tx_top.sym # of pins=8
** sym_path: xschem/tx_top.sym
** sch_path: xschem/tx_top.sch
.subckt tx_top key en_p en_n out_p out_n VDPWR VAPWR VSS
*.iopin VDPWR
*.iopin VAPWR
*.iopin VSS
*.iopin key
*.iopin en_p
*.iopin en_n
*.iopin out_p
*.iopin out_n
xring key ring VDPWR VSS tx_ring cw=3.2f
xls ring a b VDPWR VAPWR VSS tx_ls kn=14 kp=8 wpi=9 wni=3
xlse_p en_p enh_p enhb_p VDPWR VAPWR VSS tx_ls kn=1 kp=1 wpi=1 wni=0.42
xdrv_p a enh_p out_p VAPWR VSS tx_drv
xlse_n en_n enh_n enhb_n VDPWR VAPWR VSS tx_ls kn=1 kp=1 wpi=1 wni=0.42
xdrv_n b enh_n out_n VAPWR VSS tx_drv
.ends


* expanding   symbol:  decap_vapwr.sym # of pins=2
** sym_path: xschem/decap_vapwr.sym
** sch_path: xschem/decap_vapwr.sch
.subckt decap_vapwr VAPWR VGND
*.iopin VAPWR
*.iopin VGND
XMcap1 VGND VAPWR VGND VGND sky130_fd_pr__nfet_g5v0d10v5 L=5 W=18.9 nf=2 ad='int((nf+1)/2) * W/nf * 0.29'
+ as='int((nf+2)/2) * W/nf * 0.29' pd='2*int((nf+1)/2) * (W/nf + 0.29)' ps='2*int((nf+2)/2) * (W/nf + 0.29)'
+ nrd='0.29 / W' nrs='0.29 / W' sa=0 sb=0 sd=0 mult=20 m=20
XMcap2 VGND VAPWR VGND VGND sky130_fd_pr__nfet_g5v0d10v5 L=5 W=17.7 nf=2 ad='int((nf+1)/2) * W/nf * 0.29'
+ as='int((nf+2)/2) * W/nf * 0.29' pd='2*int((nf+1)/2) * (W/nf + 0.29)' ps='2*int((nf+2)/2) * (W/nf + 0.29)'
+ nrd='0.29 / W' nrs='0.29 / W' sa=0 sb=0 sd=0 mult=27 m=27
XMcap3 VGND VAPWR VGND VGND sky130_fd_pr__nfet_g5v0d10v5 L=5 W=14.7 nf=2 ad='int((nf+1)/2) * W/nf * 0.29'
+ as='int((nf+2)/2) * W/nf * 0.29' pd='2*int((nf+1)/2) * (W/nf + 0.29)' ps='2*int((nf+2)/2) * (W/nf + 0.29)'
+ nrd='0.29 / W' nrs='0.29 / W' sa=0 sb=0 sd=0 mult=12 m=12
XMcap4 VGND VAPWR VGND VGND sky130_fd_pr__nfet_g5v0d10v5 L=5 W=10.0 nf=1 ad='int((nf+1)/2) * W/nf * 0.29'
+ as='int((nf+2)/2) * W/nf * 0.29' pd='2*int((nf+1)/2) * (W/nf + 0.29)' ps='2*int((nf+2)/2) * (W/nf + 0.29)'
+ nrd='0.29 / W' nrs='0.29 / W' sa=0 sb=0 sd=0 mult=6 m=6
XMcap5 VGND VAPWR VGND VGND sky130_fd_pr__nfet_g5v0d10v5 L=5 W=8.45 nf=1 ad='int((nf+1)/2) * W/nf * 0.29'
+ as='int((nf+2)/2) * W/nf * 0.29' pd='2*int((nf+1)/2) * (W/nf + 0.29)' ps='2*int((nf+2)/2) * (W/nf + 0.29)'
+ nrd='0.29 / W' nrs='0.29 / W' sa=0 sb=0 sd=0 mult=8 m=8
XMcap6 VGND VAPWR VGND VGND sky130_fd_pr__nfet_g5v0d10v5 L=5 W=7.5 nf=2 ad='int((nf+1)/2) * W/nf * 0.29'
+ as='int((nf+2)/2) * W/nf * 0.29' pd='2*int((nf+1)/2) * (W/nf + 0.29)' ps='2*int((nf+2)/2) * (W/nf + 0.29)'
+ nrd='0.29 / W' nrs='0.29 / W' sa=0 sb=0 sd=0 mult=4 m=4
XCmim1 VAPWR VGND sky130_fd_pr__cap_mim_m3_1 W=15.58 L=17.52 MF=8 m=8
XCmim2 VAPWR VGND sky130_fd_pr__cap_mim_m3_1 W=15.58 L=10.7 MF=2 m=2
XCmim3 VAPWR VGND sky130_fd_pr__cap_mim_m3_1 W=15.08 L=16.76 MF=12 m=12
XCmim4 VAPWR VGND sky130_fd_pr__cap_mim_m3_1 W=14.47 L=16.25 MF=12 m=12
XCmim5 VAPWR VGND sky130_fd_pr__cap_mim_m3_1 W=14.44 L=18.97 MF=6 m=6
XCmim6 VAPWR VGND sky130_fd_pr__cap_mim_m3_1 W=8.8 L=18.27 MF=4 m=4
.ends


* expanding   symbol:  decap_vdpwr.sym # of pins=2
** sym_path: xschem/decap_vdpwr.sym
** sch_path: xschem/decap_vdpwr.sch
.subckt decap_vdpwr VDPWR VGND
*.iopin VDPWR
*.iopin VGND
XMcap1 VGND VDPWR VGND VGND sky130_fd_pr__nfet_01v8 L=5 W=16.2 nf=2 ad='int((nf+1)/2) * W/nf * 0.29'
+ as='int((nf+2)/2) * W/nf * 0.29' pd='2*int((nf+1)/2) * (W/nf + 0.29)' ps='2*int((nf+2)/2) * (W/nf + 0.29)'
+ nrd='0.29 / W' nrs='0.29 / W' sa=0 sb=0 sd=0 mult=20 m=20
XMcap2 VGND VDPWR VGND VGND sky130_fd_pr__nfet_01v8 L=5 W=14.3 nf=2 ad='int((nf+1)/2) * W/nf * 0.29'
+ as='int((nf+2)/2) * W/nf * 0.29' pd='2*int((nf+1)/2) * (W/nf + 0.29)' ps='2*int((nf+2)/2) * (W/nf + 0.29)'
+ nrd='0.29 / W' nrs='0.29 / W' sa=0 sb=0 sd=0 mult=3 m=3
XMcap3 VGND VDPWR VGND VGND sky130_fd_pr__nfet_01v8 L=5 W=7.3 nf=1 ad='int((nf+1)/2) * W/nf * 0.29' as='int((nf+2)/2) * W/nf * 0.29'
+ pd='2*int((nf+1)/2) * (W/nf + 0.29)' ps='2*int((nf+2)/2) * (W/nf + 0.29)' nrd='0.29 / W' nrs='0.29 / W'
+ sa=0 sb=0 sd=0 mult=2 m=2
XMcap4 VGND VDPWR VGND VGND sky130_fd_pr__nfet_01v8 L=5 W=5.3 nf=2 ad='int((nf+1)/2) * W/nf * 0.29' as='int((nf+2)/2) * W/nf * 0.29'
+ pd='2*int((nf+1)/2) * (W/nf + 0.29)' ps='2*int((nf+2)/2) * (W/nf + 0.29)' nrd='0.29 / W' nrs='0.29 / W'
+ sa=0 sb=0 sd=0 mult=1 m=1
XCmim1 VDPWR VGND sky130_fd_pr__cap_mim_m3_1 W=16.37 L=13.37 MF=12 m=12
.ends


* expanding   symbol:  amp_dp.sym # of pins=7
** sym_path: xschem/amp_dp.sym
** sch_path: xschem/amp_dp.sch
.subckt amp_dp inp inn nb outp outn VDD VSS  w=80 l=0.15 rl=1k wt=6 mt=20 mm=0
*.iopin VDD
*.iopin VSS
*.iopin nb
*.iopin inp
*.iopin inn
*.iopin outp
*.iopin outn
XRl_p outn VDD VSS sky130_fd_pr__res_high_po_1p41 L='max((rl-278)/230.3,0.5)' mult=1 m=1
XMp outn inp tail VSS sky130_fd_pr__nfet_01v8 L='l' W='w*(1+mm/2)' nf=4 ad='int((nf+1)/2) * W/nf * 0.29'
+ as='int((nf+2)/2) * W/nf * 0.29' pd='2*int((nf+1)/2) * (W/nf + 0.29)' ps='2*int((nf+2)/2) * (W/nf + 0.29)'
+ nrd='0.29 / W' nrs='0.29 / W' sa=0 sb=0 sd=0 mult=1 m=1
XRl_n outp VDD VSS sky130_fd_pr__res_high_po_1p41 L='max((rl-278)/230.3,0.5)' mult=1 m=1
XMn outp inn tail VSS sky130_fd_pr__nfet_01v8 L='l' W='w*(1-mm/2)' nf=4 ad='int((nf+1)/2) * W/nf * 0.29'
+ as='int((nf+2)/2) * W/nf * 0.29' pd='2*int((nf+1)/2) * (W/nf + 0.29)' ps='2*int((nf+2)/2) * (W/nf + 0.29)'
+ nrd='0.29 / W' nrs='0.29 / W' sa=0 sb=0 sd=0 mult=1 m=1
XMtail tail nb VSS VSS sky130_fd_pr__nfet_01v8 L=0.5 W='wt' nf=2 ad='int((nf+1)/2) * W/nf * 0.29' as='int((nf+2)/2) * W/nf * 0.29'
+ pd='2*int((nf+1)/2) * (W/nf + 0.29)' ps='2*int((nf+2)/2) * (W/nf + 0.29)' nrd='0.29 / W' nrs='0.29 / W'
+ sa=0 sb=0 sd=0 mult='mt' m='mt'
.ends


* expanding   symbol:  amp_dpc.sym # of pins=7
** sym_path: xschem/amp_dpc.sym
** sch_path: xschem/amp_dpc.sch
.subckt amp_dpc inp inn nb outp outn VDD VSS  w=20 l=0.15 rl=4k wt=6 mt=6 cs=0.6p
*.iopin VDD
*.iopin VSS
*.iopin nb
*.iopin inp
*.iopin inn
*.iopin outp
*.iopin outn
XRl_p outn VDD VSS sky130_fd_pr__res_high_po_0p69 L='max((rl-526)/470.9,0.5)' mult=1 m=1
XMp outn inp sp VSS sky130_fd_pr__nfet_01v8 L='l' W='w*(1+mm/2)' nf=4 ad='int((nf+1)/2) * W/nf * 0.29'
+ as='int((nf+2)/2) * W/nf * 0.29' pd='2*int((nf+1)/2) * (W/nf + 0.29)' ps='2*int((nf+2)/2) * (W/nf + 0.29)'
+ nrd='0.29 / W' nrs='0.29 / W' sa=0 sb=0 sd=0 mult=1 m=1
XMtail_p sp nb VSS VSS sky130_fd_pr__nfet_01v8 L=0.5 W='wt' nf=2 ad='int((nf+1)/2) * W/nf * 0.29' as='int((nf+2)/2) * W/nf * 0.29'
+ pd='2*int((nf+1)/2) * (W/nf + 0.29)' ps='2*int((nf+2)/2) * (W/nf + 0.29)' nrd='0.29 / W' nrs='0.29 / W'
+ sa=0 sb=0 sd=0 mult='mt/2' m='mt/2'
XRl_n outp VDD VSS sky130_fd_pr__res_high_po_0p69 L='max((rl-526)/470.9,0.5)' mult=1 m=1
XMn outp inn sn VSS sky130_fd_pr__nfet_01v8 L='l' W='w*(1-mm/2)' nf=4 ad='int((nf+1)/2) * W/nf * 0.29'
+ as='int((nf+2)/2) * W/nf * 0.29' pd='2*int((nf+1)/2) * (W/nf + 0.29)' ps='2*int((nf+2)/2) * (W/nf + 0.29)'
+ nrd='0.29 / W' nrs='0.29 / W' sa=0 sb=0 sd=0 mult=1 m=1
XMtail_n sn nb VSS VSS sky130_fd_pr__nfet_01v8 L=0.5 W='wt' nf=2 ad='int((nf+1)/2) * W/nf * 0.29' as='int((nf+2)/2) * W/nf * 0.29'
+ pd='2*int((nf+1)/2) * (W/nf + 0.29)' ps='2*int((nf+2)/2) * (W/nf + 0.29)' nrd='0.29 / W' nrs='0.29 / W'
+ sa=0 sb=0 sd=0 mult='mt/2' m='mt/2'
XCs_a sn sp sky130_fd_pr__cap_mim_m3_1 W='sqrt((cs/2)/2.06e-15/3.13676)' L='3.13676*sqrt((cs/2)/2.06e-15/3.13676)'
+ MF=1 m=1
XCs_b sp sn sky130_fd_pr__cap_mim_m3_1 W='sqrt((cs/2)/2.06e-15/3.13676)' L='3.13676*sqrt((cs/2)/2.06e-15/3.13676)'
+ MF=1 m=1
.ends


* expanding   symbol:  lna_shunt.sym # of pins=5
** sym_path: xschem/lna_shunt.sym
** sch_path: xschem/lna_shunt.sch
.subckt lna_shunt a b g VDD VSS  rh=421 wsw=18 rg=20k
*.iopin VDD
*.iopin VSS
*.iopin a
*.iopin b
*.iopin g
XRh_a sa a VSS sky130_fd_pr__res_high_po_1p41 L='max((rh-278)/230.3,0.5)' mult=1 m=1
XRh_b b sb VSS sky130_fd_pr__res_high_po_1p41 L='max((rh-278)/230.3,0.5)' mult=1 m=1
XMsw sb gi sa VDD sky130_fd_pr__pfet_01v8 L=0.15 W='wsw' nf=6 ad='int((nf+1)/2) * W/nf * 0.29' as='int((nf+2)/2) * W/nf * 0.29'
+ pd='2*int((nf+1)/2) * (W/nf + 0.29)' ps='2*int((nf+2)/2) * (W/nf + 0.29)' nrd='0.29 / W' nrs='0.29 / W'
+ sa=0 sb=0 sd=0 mult=1 m=1
XRg g gi VSS sky130_fd_pr__res_xhigh_po_0p35 L='max((rg-0)/7379,0.5)' mult=1 m=1
XMcap VDD gi VDD VDD sky130_fd_pr__pfet_01v8 L=5 W=5 nf=1 ad='int((nf+1)/2) * W/nf * 0.29' as='int((nf+2)/2) * W/nf * 0.29'
+ pd='2*int((nf+1)/2) * (W/nf + 0.29)' ps='2*int((nf+2)/2) * (W/nf + 0.29)' nrd='0.29 / W' nrs='0.29 / W'
+ sa=0 sb=0 sd=0 mult=1 m=1
.ends


* expanding   symbol:  det_cell.sym # of pins=5
** sym_path: xschem/det_cell.sym
** sch_path: xschem/det_cell.sch
.subckt det_cell inp inn vb out VSS  wd=1 rs=10k cc=100f rb=200k
*.iopin VSS
*.iopin vb
*.iopin inp
*.iopin inn
*.iopin out
XCc_p gp inp sky130_fd_pr__cap_mim_m3_1 W='sqrt((cc)/1/2.06e-15)' L='sqrt((cc)/1/2.06e-15)' MF=1 m=1
XRb_p gp vb VSS sky130_fd_pr__res_xhigh_po_0p35 L='max((rb-0)/7379,0.5)' mult=1 m=1
XMp out gp sp VSS sky130_fd_pr__nfet_01v8 L=0.15 W='wd' nf=1 ad='int((nf+1)/2) * W/nf * 0.29' as='int((nf+2)/2) * W/nf * 0.29'
+ pd='2*int((nf+1)/2) * (W/nf + 0.29)' ps='2*int((nf+2)/2) * (W/nf + 0.29)' nrd='0.29 / W' nrs='0.29 / W'
+ sa=0 sb=0 sd=0 mult=1 m=1
XRs_p VSS sp VSS sky130_fd_pr__res_high_po_0p35 L='max((rs-963)/995,0.5)' mult=1 m=1
XCc_n gn inn sky130_fd_pr__cap_mim_m3_1 W='sqrt((cc)/1/2.06e-15)' L='sqrt((cc)/1/2.06e-15)' MF=1 m=1
XRb_n gn vb VSS sky130_fd_pr__res_xhigh_po_0p35 L='max((rb-0)/7379,0.5)' mult=1 m=1
XMn out gn sn VSS sky130_fd_pr__nfet_01v8 L=0.15 W='wd' nf=1 ad='int((nf+1)/2) * W/nf * 0.29' as='int((nf+2)/2) * W/nf * 0.29'
+ pd='2*int((nf+1)/2) * (W/nf + 0.29)' ps='2*int((nf+2)/2) * (W/nf + 0.29)' nrd='0.29 / W' nrs='0.29 / W'
+ sa=0 sb=0 sd=0 mult=1 m=1
XRs_n VSS sn VSS sky130_fd_pr__res_high_po_0p35 L='max((rs-963)/995,0.5)' mult=1 m=1
.ends


* expanding   symbol:  tx_ring.sym # of pins=4
** sym_path: xschem/tx_ring.sym
** sch_path: xschem/tx_ring.sch
.subckt tx_ring en out VDD VSS  cw=3.2f
*.iopin VDD
*.iopin VSS
*.iopin en
*.iopin out
xr0 en r22 VSS VSS VDD VDD out sky130_fd_sc_hd__nand2_2
Cr0 out VSS 'cw' m=1
xr1 out VSS VSS VDD VDD r1 sky130_fd_sc_hd__inv_2
Cr1 r1 VSS 'cw' m=1
xr2 r1 VSS VSS VDD VDD r2 sky130_fd_sc_hd__inv_2
Cr2 r2 VSS 'cw' m=1
xr3 r2 VSS VSS VDD VDD r3 sky130_fd_sc_hd__inv_2
Cr3 r3 VSS 'cw' m=1
xr4 r3 VSS VSS VDD VDD r4 sky130_fd_sc_hd__inv_2
Cr4 r4 VSS 'cw' m=1
xr5 r4 VSS VSS VDD VDD r5 sky130_fd_sc_hd__inv_2
Cr5 r5 VSS 'cw' m=1
xr6 r5 VSS VSS VDD VDD r6 sky130_fd_sc_hd__inv_2
Cr6 r6 VSS 'cw' m=1
xr7 r6 VSS VSS VDD VDD r7 sky130_fd_sc_hd__inv_2
Cr7 r7 VSS 'cw' m=1
xr8 r7 VSS VSS VDD VDD r8 sky130_fd_sc_hd__inv_2
Cr8 r8 VSS 'cw' m=1
xr9 r8 VSS VSS VDD VDD r9 sky130_fd_sc_hd__inv_2
Cr9 r9 VSS 'cw' m=1
xr10 r9 VSS VSS VDD VDD r10 sky130_fd_sc_hd__inv_2
Cr10 r10 VSS 'cw' m=1
xr11 r10 VSS VSS VDD VDD r11 sky130_fd_sc_hd__inv_2
Cr11 r11 VSS 'cw' m=1
xr12 r11 VSS VSS VDD VDD r12 sky130_fd_sc_hd__inv_2
Cr12 r12 VSS 'cw' m=1
xr13 r12 VSS VSS VDD VDD r13 sky130_fd_sc_hd__inv_2
Cr13 r13 VSS 'cw' m=1
xr14 r13 VSS VSS VDD VDD r14 sky130_fd_sc_hd__inv_2
Cr14 r14 VSS 'cw' m=1
xr15 r14 VSS VSS VDD VDD r15 sky130_fd_sc_hd__inv_2
Cr15 r15 VSS 'cw' m=1
xr16 r15 VSS VSS VDD VDD r16 sky130_fd_sc_hd__inv_2
Cr16 r16 VSS 'cw' m=1
xr17 r16 VSS VSS VDD VDD r17 sky130_fd_sc_hd__inv_2
Cr17 r17 VSS 'cw' m=1
xr18 r17 VSS VSS VDD VDD r18 sky130_fd_sc_hd__inv_2
Cr18 r18 VSS 'cw' m=1
xr19 r18 VSS VSS VDD VDD r19 sky130_fd_sc_hd__inv_2
Cr19 r19 VSS 'cw' m=1
xr20 r19 VSS VSS VDD VDD r20 sky130_fd_sc_hd__inv_2
Cr20 r20 VSS 'cw' m=1
xr21 r20 VSS VSS VDD VDD r21 sky130_fd_sc_hd__inv_2
Cr21 r21 VSS 'cw' m=1
xr22 r21 VSS VSS VDD VDD r22 sky130_fd_sc_hd__inv_2
Cr22 r22 VSS 'cw' m=1
.ends


* expanding   symbol:  tx_ls.sym # of pins=6
** sym_path: xschem/tx_ls.sym
** sch_path: xschem/tx_ls.sch
.subckt tx_ls in A B VDD VAPWR VSS  kn=14 kp=8 wpi=9 wni=3
*.iopin VDD
*.iopin VAPWR
*.iopin VSS
*.iopin in
*.iopin A
*.iopin B
XMi1p ctrl in VDD VDD sky130_fd_pr__pfet_01v8 L=0.15 W='wpi' nf=1 ad='int((nf+1)/2) * W/nf * 0.29' as='int((nf+2)/2) * W/nf * 0.29'
+ pd='2*int((nf+1)/2) * (W/nf + 0.29)' ps='2*int((nf+2)/2) * (W/nf + 0.29)' nrd='0.29 / W' nrs='0.29 / W'
+ sa=0 sb=0 sd=0 mult=1 m=1
XMi1n ctrl in VSS VSS sky130_fd_pr__nfet_01v8 L=0.15 W='wni' nf=1 ad='int((nf+1)/2) * W/nf * 0.29' as='int((nf+2)/2) * W/nf * 0.29'
+ pd='2*int((nf+1)/2) * (W/nf + 0.29)' ps='2*int((nf+2)/2) * (W/nf + 0.29)' nrd='0.29 / W' nrs='0.29 / W'
+ sa=0 sb=0 sd=0 mult=1 m=1
XM8 ctrl_n ctrl VDD VDD sky130_fd_pr__pfet_01v8_hvt L=0.15 W=4 nf=1 ad='int((nf+1)/2) * W/nf * 0.29'
+ as='int((nf+2)/2) * W/nf * 0.29' pd='2*int((nf+1)/2) * (W/nf + 0.29)' ps='2*int((nf+2)/2) * (W/nf + 0.29)'
+ nrd='0.29 / W' nrs='0.29 / W' sa=0 sb=0 sd=0 mult=1 m=1
XM7 ctrl_n ctrl VSS VSS sky130_fd_pr__nfet_01v8 L=0.15 W=1.68 nf=1 ad='int((nf+1)/2) * W/nf * 0.29' as='int((nf+2)/2) * W/nf * 0.29'
+ pd='2*int((nf+1)/2) * (W/nf + 0.29)' ps='2*int((nf+2)/2) * (W/nf + 0.29)' nrd='0.29 / W' nrs='0.29 / W'
+ sa=0 sb=0 sd=0 mult=1 m=1
XM9 A ctrl VSS VSS sky130_fd_pr__nfet_g5v0d10v5 L=0.5 W='0.42*kn' nf=1 ad='int((nf+1)/2) * W/nf * 0.29'
+ as='int((nf+2)/2) * W/nf * 0.29' pd='2*int((nf+1)/2) * (W/nf + 0.29)' ps='2*int((nf+2)/2) * (W/nf + 0.29)'
+ nrd='0.29 / W' nrs='0.29 / W' sa=0 sb=0 sd=0 mult=1 m=1
XM10 B ctrl_n VSS VSS sky130_fd_pr__nfet_g5v0d10v5 L=0.5 W='0.42*kn' nf=1 ad='int((nf+1)/2) * W/nf * 0.29'
+ as='int((nf+2)/2) * W/nf * 0.29' pd='2*int((nf+1)/2) * (W/nf + 0.29)' ps='2*int((nf+2)/2) * (W/nf + 0.29)'
+ nrd='0.29 / W' nrs='0.29 / W' sa=0 sb=0 sd=0 mult=1 m=1
XM11 A B VAPWR VAPWR sky130_fd_pr__pfet_g5v0d10v5 L=0.5 W='0.42*kp' nf=1 ad='int((nf+1)/2) * W/nf * 0.29'
+ as='int((nf+2)/2) * W/nf * 0.29' pd='2*int((nf+1)/2) * (W/nf + 0.29)' ps='2*int((nf+2)/2) * (W/nf + 0.29)'
+ nrd='0.29 / W' nrs='0.29 / W' sa=0 sb=0 sd=0 mult=1 m=1
XM12 B A VAPWR VAPWR sky130_fd_pr__pfet_g5v0d10v5 L=0.5 W='0.42*kp' nf=1 ad='int((nf+1)/2) * W/nf * 0.29'
+ as='int((nf+2)/2) * W/nf * 0.29' pd='2*int((nf+1)/2) * (W/nf + 0.29)' ps='2*int((nf+2)/2) * (W/nf + 0.29)'
+ nrd='0.29 / W' nrs='0.29 / W' sa=0 sb=0 sd=0 mult=1 m=1
.ends


* expanding   symbol:  tx_drv.sym # of pins=5
** sym_path: xschem/tx_drv.sym
** sch_path: xschem/tx_drv.sch
.subckt tx_drv in en out VAPWR VSS
*.iopin VAPWR
*.iopin VSS
*.iopin in
*.iopin en
*.iopin out
XMnap y0 in VAPWR VAPWR sky130_fd_pr__pfet_g5v0d10v5 L=0.5 W=1.26 nf=1 ad='int((nf+1)/2) * W/nf * 0.29'
+ as='int((nf+2)/2) * W/nf * 0.29' pd='2*int((nf+1)/2) * (W/nf + 0.29)' ps='2*int((nf+2)/2) * (W/nf + 0.29)'
+ nrd='0.29 / W' nrs='0.29 / W' sa=0 sb=0 sd=0 mult=1 m=1
XMnbp y0 en VAPWR VAPWR sky130_fd_pr__pfet_g5v0d10v5 L=0.5 W=1.26 nf=1 ad='int((nf+1)/2) * W/nf * 0.29'
+ as='int((nf+2)/2) * W/nf * 0.29' pd='2*int((nf+1)/2) * (W/nf + 0.29)' ps='2*int((nf+2)/2) * (W/nf + 0.29)'
+ nrd='0.29 / W' nrs='0.29 / W' sa=0 sb=0 sd=0 mult=1 m=1
XMnan y0 in ns VSS sky130_fd_pr__nfet_g5v0d10v5 L=0.5 W=0.84 nf=1 ad='int((nf+1)/2) * W/nf * 0.29' as='int((nf+2)/2) * W/nf * 0.29'
+ pd='2*int((nf+1)/2) * (W/nf + 0.29)' ps='2*int((nf+2)/2) * (W/nf + 0.29)' nrd='0.29 / W' nrs='0.29 / W'
+ sa=0 sb=0 sd=0 mult=1 m=1
XMnbn ns en VSS VSS sky130_fd_pr__nfet_g5v0d10v5 L=0.5 W=0.84 nf=1 ad='int((nf+1)/2) * W/nf * 0.29' as='int((nf+2)/2) * W/nf * 0.29'
+ pd='2*int((nf+1)/2) * (W/nf + 0.29)' ps='2*int((nf+2)/2) * (W/nf + 0.29)' nrd='0.29 / W' nrs='0.29 / W'
+ sa=0 sb=0 sd=0 mult=1 m=1
XM1p y1 y0 VAPWR VAPWR sky130_fd_pr__pfet_g5v0d10v5 L=0.5 W=1.26 nf=1 ad='int((nf+1)/2) * W/nf * 0.29'
+ as='int((nf+2)/2) * W/nf * 0.29' pd='2*int((nf+1)/2) * (W/nf + 0.29)' ps='2*int((nf+2)/2) * (W/nf + 0.29)'
+ nrd='0.29 / W' nrs='0.29 / W' sa=0 sb=0 sd=0 mult=1 m=1
XM1n y1 y0 VSS VSS sky130_fd_pr__nfet_g5v0d10v5 L=0.5 W=0.42 nf=1 ad='int((nf+1)/2) * W/nf * 0.29' as='int((nf+2)/2) * W/nf * 0.29'
+ pd='2*int((nf+1)/2) * (W/nf + 0.29)' ps='2*int((nf+2)/2) * (W/nf + 0.29)' nrd='0.29 / W' nrs='0.29 / W'
+ sa=0 sb=0 sd=0 mult=1 m=1
XM2p y2 y1 VAPWR VAPWR sky130_fd_pr__pfet_g5v0d10v5 L=0.5 W=5.04 nf=1 ad='int((nf+1)/2) * W/nf * 0.29'
+ as='int((nf+2)/2) * W/nf * 0.29' pd='2*int((nf+1)/2) * (W/nf + 0.29)' ps='2*int((nf+2)/2) * (W/nf + 0.29)'
+ nrd='0.29 / W' nrs='0.29 / W' sa=0 sb=0 sd=0 mult=1 m=1
XM2n y2 y1 VSS VSS sky130_fd_pr__nfet_g5v0d10v5 L=0.5 W=1.68 nf=1 ad='int((nf+1)/2) * W/nf * 0.29' as='int((nf+2)/2) * W/nf * 0.29'
+ pd='2*int((nf+1)/2) * (W/nf + 0.29)' ps='2*int((nf+2)/2) * (W/nf + 0.29)' nrd='0.29 / W' nrs='0.29 / W'
+ sa=0 sb=0 sd=0 mult=1 m=1
XM3p y3 y2 VAPWR VAPWR sky130_fd_pr__pfet_g5v0d10v5 L=0.5 W=20.16 nf=2 ad='int((nf+1)/2) * W/nf * 0.29'
+ as='int((nf+2)/2) * W/nf * 0.29' pd='2*int((nf+1)/2) * (W/nf + 0.29)' ps='2*int((nf+2)/2) * (W/nf + 0.29)'
+ nrd='0.29 / W' nrs='0.29 / W' sa=0 sb=0 sd=0 mult=1 m=1
XM3n y3 y2 VSS VSS sky130_fd_pr__nfet_g5v0d10v5 L=0.5 W=6.72 nf=1 ad='int((nf+1)/2) * W/nf * 0.29' as='int((nf+2)/2) * W/nf * 0.29'
+ pd='2*int((nf+1)/2) * (W/nf + 0.29)' ps='2*int((nf+2)/2) * (W/nf + 0.29)' nrd='0.29 / W' nrs='0.29 / W'
+ sa=0 sb=0 sd=0 mult=1 m=1
XM4p y4 y3 VAPWR VAPWR sky130_fd_pr__pfet_g5v0d10v5 L=0.5 W=80.64 nf=8 ad='int((nf+1)/2) * W/nf * 0.29'
+ as='int((nf+2)/2) * W/nf * 0.29' pd='2*int((nf+1)/2) * (W/nf + 0.29)' ps='2*int((nf+2)/2) * (W/nf + 0.29)'
+ nrd='0.29 / W' nrs='0.29 / W' sa=0 sb=0 sd=0 mult=1 m=1
XM4n y4 y3 VSS VSS sky130_fd_pr__nfet_g5v0d10v5 L=0.5 W=26.88 nf=3 ad='int((nf+1)/2) * W/nf * 0.29' as='int((nf+2)/2) * W/nf * 0.29'
+ pd='2*int((nf+1)/2) * (W/nf + 0.29)' ps='2*int((nf+2)/2) * (W/nf + 0.29)' nrd='0.29 / W' nrs='0.29 / W'
+ sa=0 sb=0 sd=0 mult=1 m=1
XM5p out y4 VAPWR VAPWR sky130_fd_pr__pfet_g5v0d10v5 L=0.5 W=144 nf=14 ad='int((nf+1)/2) * W/nf * 0.29'
+ as='int((nf+2)/2) * W/nf * 0.29' pd='2*int((nf+1)/2) * (W/nf + 0.29)' ps='2*int((nf+2)/2) * (W/nf + 0.29)'
+ nrd='0.29 / W' nrs='0.29 / W' sa=0 sb=0 sd=0 mult=1 m=1
XM5n out y4 VSS VSS sky130_fd_pr__nfet_g5v0d10v5 L=0.5 W=48 nf=5 ad='int((nf+1)/2) * W/nf * 0.29' as='int((nf+2)/2) * W/nf * 0.29'
+ pd='2*int((nf+1)/2) * (W/nf + 0.29)' ps='2*int((nf+2)/2) * (W/nf + 0.29)' nrd='0.29 / W' nrs='0.29 / W'
+ sa=0 sb=0 sd=0 mult=1 m=1
.ends

.end
